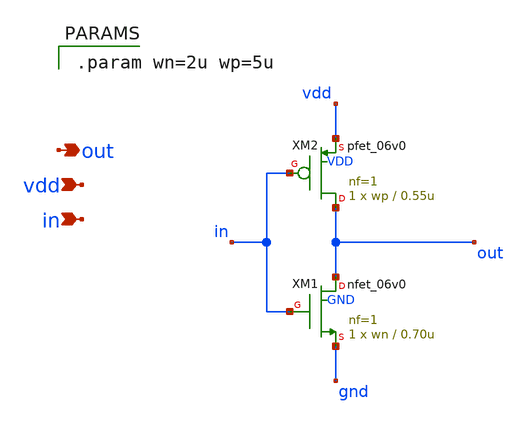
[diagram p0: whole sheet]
** sch_path: Schematics #2/xschem/inv.sch
**.subckt inv out vdd in
*.opin out
*.ipin vdd
*.ipin in
XM1 out in gnd GND nfet_06v0 L=0.70u W=wn nf=1 ad='int((nf+1)/2) * W/nf * 0.18u' as='int((nf+2)/2) * W/nf * 0.18u'
+ pd='2*int((nf+1)/2) * (W/nf + 0.18u)' ps='2*int((nf+2)/2) * (W/nf + 0.18u)' nrd='0.18u / W' nrs='0.18u / W'
+ sa=0 sb=0 sd=0 m=1 par=1
XM2 out in vdd VDD pfet_06v0 L=0.55u W=wp nf=1 ad='int((nf+1)/2) * W/nf * 0.18u' as='int((nf+2)/2) * W/nf * 0.18u'
+ pd='2*int((nf+1)/2) * (W/nf + 0.18u)' ps='2*int((nf+2)/2) * (W/nf + 0.18u)' nrd='0.18u / W' nrs='0.18u / W'
+ sa=0 sb=0 sd=0 m=1 par=1
**** begin user architecture code

.param wn=2u wp=5u

**** end user architecture code
**.ends
.end
